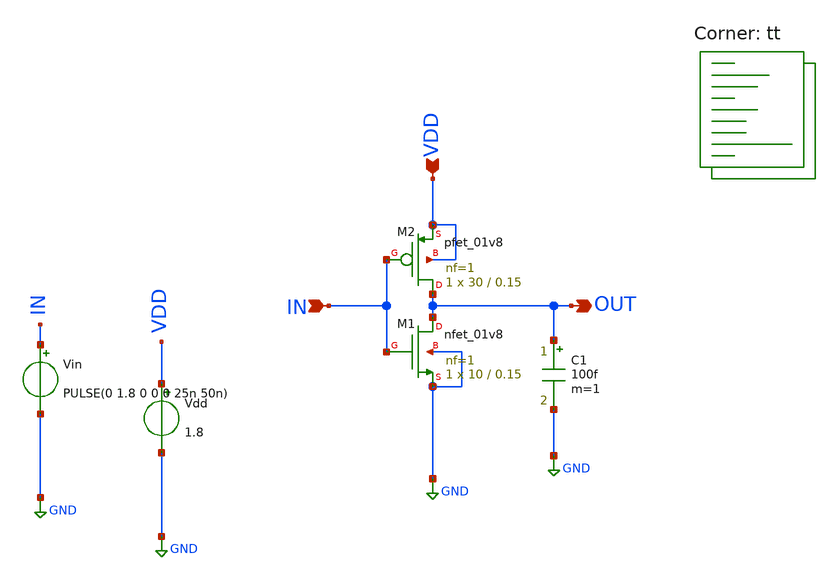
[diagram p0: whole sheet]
** sch_path: sizing-inverter.sch
**.subckt sizing-inverter IN VDD OUT
*.ipin IN
*.ipin VDD
*.opin OUT
Vin IN GND PULSE(0 1.8 0 0 0 25n 50n)
Vdd VDD GND 1.8
XM1 OUT IN GND GND sky130_fd_pr__nfet_01v8 L=0.15 W=10 nf=1 ad='int((nf+1)/2) * W/nf * 0.29' as='int((nf+2)/2) * W/nf * 0.29'
+ pd='2*int((nf+1)/2) * (W/nf + 0.29)' ps='2*int((nf+2)/2) * (W/nf + 0.29)' nrd='0.29 / W' nrs='0.29 / W'
+ sa=0 sb=0 sd=0 mult=1 m=1
XM2 OUT IN VDD VDD sky130_fd_pr__pfet_01v8 L=0.15 W=30 nf=1 ad='int((nf+1)/2) * W/nf * 0.29' as='int((nf+2)/2) * W/nf * 0.29'
+ pd='2*int((nf+1)/2) * (W/nf + 0.29)' ps='2*int((nf+2)/2) * (W/nf + 0.29)' nrd='0.29 / W' nrs='0.29 / W'
+ sa=0 sb=0 sd=0 mult=1 m=1
C1 OUT GND 100f m=1
**** begin user architecture code
.lib $::SKYWATER_MODELS/sky130.lib.spice tt


.options savecurrents

.control
save all

let step=1
let max_w=80
let curr_w=10

let iters = ceil((max_w - curr_w)/step)
let iter = 0

let switching_points = vector(iters)
let diffs = vector(iters)
let width = vector(iters)


while curr_w < max_w

	alter m.xm2.msky130_fd_pr__pfet_01v8 W=curr_w

******* Asymmetricity analysis ********
	tran 10p 50n ; Run transient analysis using a symmetric pulse of period 25n

	meas tran rise_time TRIG v(out) VAL=0.1 RISE=1 TARG v(out) VAL=1.62 RISE=1
	meas tran fall_time TRIG v(out) VAL=1.62 FALL=1 TARG v(out) VAL=0.1 FALL=1

	let diffs[iter] = abs( $&rise_time - $&fall_time ) ; Create array of diffs



******* Switching point analysis ********
	dc vin 0 1.8 1m ; Run dc analysis, check for operating point

	meas dc switching_point WHEN v(out)=v(in) CROSS=LAST
	set plotstr = ( $plotstr {$curplot}.v(out) )
	set global_switching_point = $&switching_point

	let switching_points[iter] = $&switching_point
	let width[iter] = curr_w


	let curr_w=curr_w + step
	let iter=iter + 1

	end

set plotstr = ( $plotstr {$curplot}.v(in) )

set nolegend

******* Plot results ********
plot switching_points vs width title 'switching points vs time' xlabel 'width' ylabel 'Switching point (V)'
plot diffs vs width title 'asymmetricity vs time' xlabel 'width' ylabel 'Difference in rise/fall'

plot $plotstr

******* Find switching point at most symmetric w ********
let lowest_asym = 100
let best_w_index = 0 ; Find most symmetric w
let iter = 0
let tolerance = 1p ; We let the asymmetricity be plus/minus 1p of 0

repeat $&iters

  let asym = abs(diffs[iter] - 1p)
  let curr_w = width[iter]

  if asym < lowest_asym ; If we have something smaller, set it as the best goal and repeat
    let best_w_index = iter
    let lowest_asym = asym

  end

  let iter = iter + 1
end

* Now that we have the best width, we now need to move towards getting the switching point

let chosen_switching_point = switching_points[best_w_index]

.endc


**** end user architecture code
**.ends
.GLOBAL GND
.end
